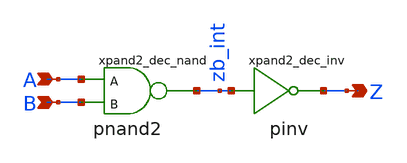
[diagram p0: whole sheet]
** sch_path: sram_2_64_scn4m_lcc/and2_dec.sch
**.subckt and2_dec A B Z
*.ipin A
*.ipin B
*.opin Z
xpand2_dec_nand A B zb_int vdd gnd pnand2
xpand2_dec_inv zb_int Z vdd gnd pinv
**.ends
.end
